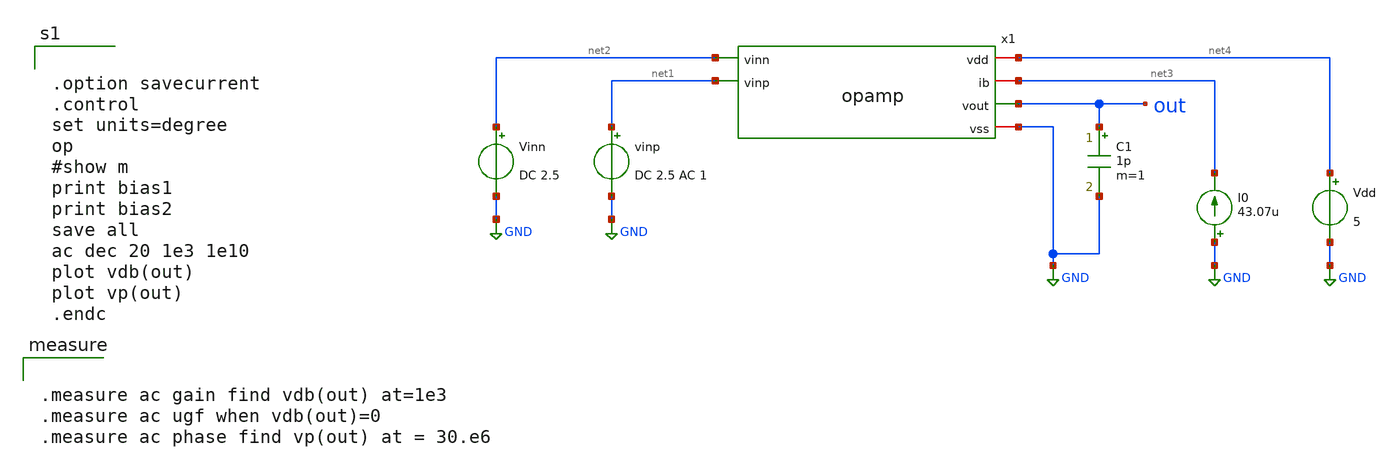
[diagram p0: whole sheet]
** sch_path: member_project/GroupWork/Team_masahiro/opamp_ac.sch
**.subckt opamp_ac
x1 net4 net3 net2 net1 out GND opamp
Vinn net2 GND DC 2.5
vinp net1 GND DC 2.5 AC 1
I0 GND net3 43.07u
Vdd net4 GND 5
C1 out GND 1p m=1
**** begin user architecture code
 .include $::LIB/mos.lib
.include $::LIB/passive.lib
.include $::LIB/diode.lib


.option savecurrent
.control
set units=degree
op
#show m
print bias1
print bias2
save all
ac dec 20 1e3 1e10
plot vdb(out)
plot vp(out)
.endc




.measure ac gain find vdb(out) at=1e3
.measure ac ugf when vdb(out)=0
.measure ac phase find vp(out) at = 30.e6


**** end user architecture code
**.ends

* expanding   symbol:  opamp.sym # of pins=6
** sym_path: member_project/GroupWork/Team_masahiro/opamp.sym
** sch_path: member_project/GroupWork/Team_masahiro/opamp.sch
.subckt opamp vdd ib vinn vinp vout vss
*.ipin vinn
*.ipin vinp
*.iopin vss
*.iopin vdd
*.opin vout
*.iopin ib
M1 ib ib vss vss nmos L=2u W=20u m=1
M2 net1 ib vss vss nmos L=2u W=20u m=1
M3 net1 net1 vdd vdd pmos L=2u W=20u m=1
M4 net3 net1 vdd vdd pmos L=2u W=20u m=1
M5 net3 net3 net2 vss nmos L=1u W=14u m=1
M6 net2 net2 vss vss nmos L=1u W=14u m=1
M7 net4 vinn net6 vss nmos L=2u W=100u m=1
M8 net5 vinp net6 vss nmos L=2u W=100u m=1
M9 net6 ib vss vss nmos L=2u W=20u m=1
M10 net4 net4 vdd vdd pmos L=2u W=35u m=1
M11 net5 net4 vdd vdd pmos L=2u W=35u m=1
M12 vout ib vss vss nmos L=1u W=80u m=1
M13 net7 net5 vdd vdd pmos L=1u W=160u m=1
M14 vout net3 net7 net7 pmos L=1u W=160u m=1
C1 vout net8 poly_cap W=26 L=26
R1 net5 net8 R_poly W=1 L=300
.ends

.GLOBAL GND
.end
